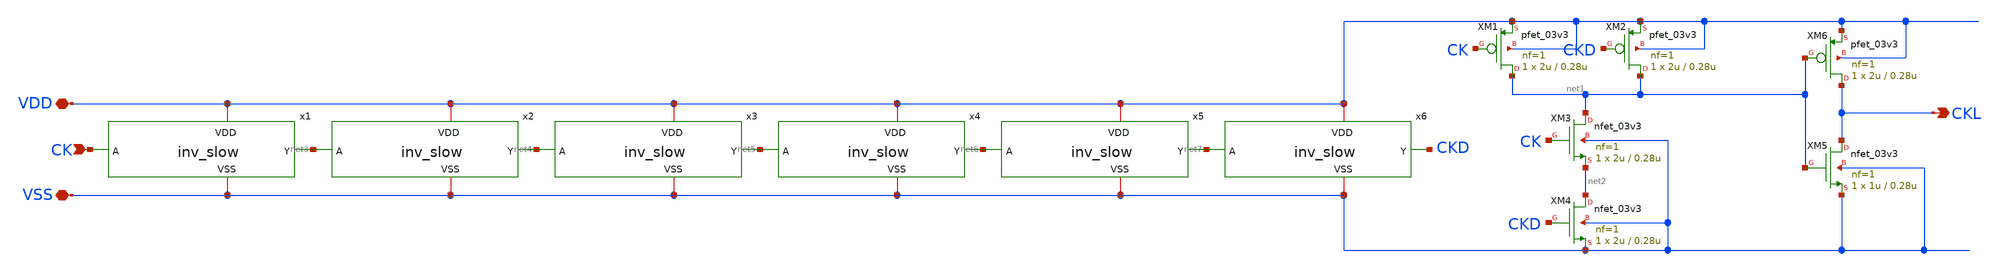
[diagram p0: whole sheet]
** sch_path: comparator_alt/schematic/ckl_gen.sch
**.subckt ckl_gen VDD VSS CK CKL
*.iopin VDD
*.iopin VSS
*.ipin CK
*.opin CKL
x1 VDD net3 CK VSS inv_slow
x2 VDD net4 net3 VSS inv_slow
x3 VDD net5 net4 VSS inv_slow
x4 VDD net6 net5 VSS inv_slow
x5 VDD net7 net6 VSS inv_slow
x6 VDD CKD net7 VSS inv_slow
XM1 net1 CK VDD VDD pfet_03v3 L=0.28u W=2u nf=1 ad='int((nf+1)/2) * W/nf * 0.18u' as='int((nf+2)/2) * W/nf * 0.18u'
+ pd='2*int((nf+1)/2) * (W/nf + 0.18u)' ps='2*int((nf+2)/2) * (W/nf + 0.18u)' nrd='0.18u / W' nrs='0.18u / W'
+ sa=0 sb=0 sd=0 m=1
XM2 net1 CKD VDD VDD pfet_03v3 L=0.28u W=2u nf=1 ad='int((nf+1)/2) * W/nf * 0.18u' as='int((nf+2)/2) * W/nf * 0.18u'
+ pd='2*int((nf+1)/2) * (W/nf + 0.18u)' ps='2*int((nf+2)/2) * (W/nf + 0.18u)' nrd='0.18u / W' nrs='0.18u / W'
+ sa=0 sb=0 sd=0 m=1
XM3 net1 CK net2 VSS nfet_03v3 L=0.28u W=2u nf=1 ad='int((nf+1)/2) * W/nf * 0.18u' as='int((nf+2)/2) * W/nf * 0.18u'
+ pd='2*int((nf+1)/2) * (W/nf + 0.18u)' ps='2*int((nf+2)/2) * (W/nf + 0.18u)' nrd='0.18u / W' nrs='0.18u / W'
+ sa=0 sb=0 sd=0 m=1
XM4 net2 CKD VSS VSS nfet_03v3 L=0.28u W=2u nf=1 ad='int((nf+1)/2) * W/nf * 0.18u' as='int((nf+2)/2) * W/nf * 0.18u'
+ pd='2*int((nf+1)/2) * (W/nf + 0.18u)' ps='2*int((nf+2)/2) * (W/nf + 0.18u)' nrd='0.18u / W' nrs='0.18u / W'
+ sa=0 sb=0 sd=0 m=1
XM5 CKL net1 VSS VSS nfet_03v3 L=0.28u W=1u nf=1 ad='int((nf+1)/2) * W/nf * 0.18u' as='int((nf+2)/2) * W/nf * 0.18u'
+ pd='2*int((nf+1)/2) * (W/nf + 0.18u)' ps='2*int((nf+2)/2) * (W/nf + 0.18u)' nrd='0.18u / W' nrs='0.18u / W'
+ sa=0 sb=0 sd=0 m=1
XM6 CKL net1 VDD VDD pfet_03v3 L=0.28u W=2u nf=1 ad='int((nf+1)/2) * W/nf * 0.18u' as='int((nf+2)/2) * W/nf * 0.18u'
+ pd='2*int((nf+1)/2) * (W/nf + 0.18u)' ps='2*int((nf+2)/2) * (W/nf + 0.18u)' nrd='0.18u / W' nrs='0.18u / W'
+ sa=0 sb=0 sd=0 m=1
**.ends

* expanding   symbol:  comparator_alt/schematic/inv_slow.sym # of pins=4
** sym_path: comparator_alt/schematic/inv_slow.sym
** sch_path: comparator_alt/schematic/inv_slow.sch
.subckt inv_slow VDD Y A VSS
*.iopin VDD
*.iopin VSS
*.opin Y
*.ipin A
XMT1 Y A VSS VSS nfet_03v3 L=1u W=1u nf=1 ad='int((nf+1)/2) * W/nf * 0.18u' as='int((nf+2)/2) * W/nf * 0.18u'
+ pd='2*int((nf+1)/2) * (W/nf + 0.18u)' ps='2*int((nf+2)/2) * (W/nf + 0.18u)' nrd='0.18u / W' nrs='0.18u / W'
+ sa=0 sb=0 sd=0 m=1
XM1 Y A VDD VDD pfet_03v3 L=1u W=2u nf=1 ad='int((nf+1)/2) * W/nf * 0.18u' as='int((nf+2)/2) * W/nf * 0.18u'
+ pd='2*int((nf+1)/2) * (W/nf + 0.18u)' ps='2*int((nf+2)/2) * (W/nf + 0.18u)' nrd='0.18u / W' nrs='0.18u / W'
+ sa=0 sb=0 sd=0 m=1
.ends

.end
